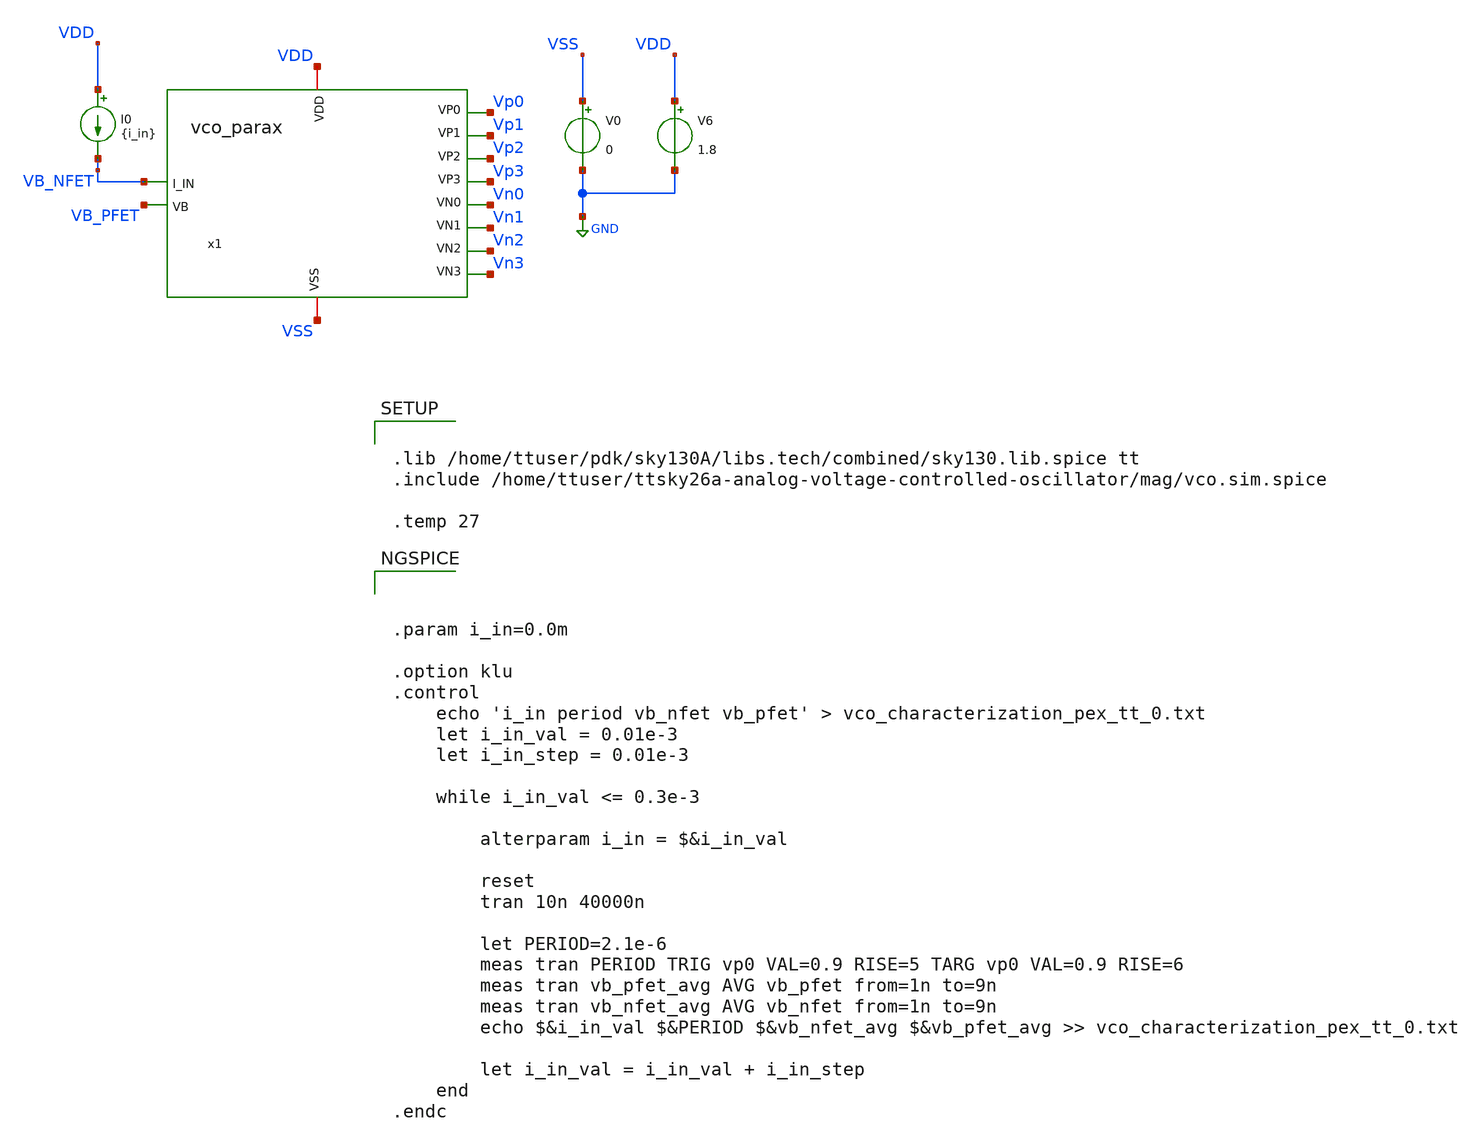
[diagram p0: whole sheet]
** sch_path: xschem/vco_characterization_tb_pex.sch
**.subckt vco_characterization_tb_pex
V0 VSS GND 0
V6 VDD GND 1.8
I0 VDD VB_NFET {i_in}
x1 VDD VSS VB_NFET Vp0 Vp1 Vp2 Vp3 Vn0 Vn1 Vn2 Vn3 VB_PFET vco_parax
**** begin user architecture code



.param i_in=0.0m

.option klu
.control
	echo 'i_in period vb_nfet vb_pfet' > vco_characterization_pex_tt_0.txt
	let i_in_val = 0.01e-3
	let i_in_step = 0.01e-3

	while i_in_val <= 0.3e-3

		alterparam i_in = $&i_in_val

		reset
		tran 10n 40000n

		let PERIOD=2.1e-6
		meas tran PERIOD TRIG vp0 VAL=0.9 RISE=5 TARG vp0 VAL=0.9 RISE=6
		meas tran vb_pfet_avg AVG vb_pfet from=1n to=9n
		meas tran vb_nfet_avg AVG vb_nfet from=1n to=9n
		echo $&i_in_val $&PERIOD $&vb_nfet_avg $&vb_pfet_avg >> vco_characterization_pex_tt_0.txt

		let i_in_val = i_in_val + i_in_step
	end
.endc




.lib /home/ttuser/pdk/sky130A/libs.tech/combined/sky130.lib.spice tt
.include /home/ttuser/ttsky26a-analog-voltage-controlled-oscillator/mag/vco.sim.spice

.temp 27


**** end user architecture code
**.ends

* expanding   symbol:  vco_parax.sym # of pins=12
** sym_path: xschem/vco.sym
.include [file normalize ../mag/vco.sim.spice]
.GLOBAL GND
.end
